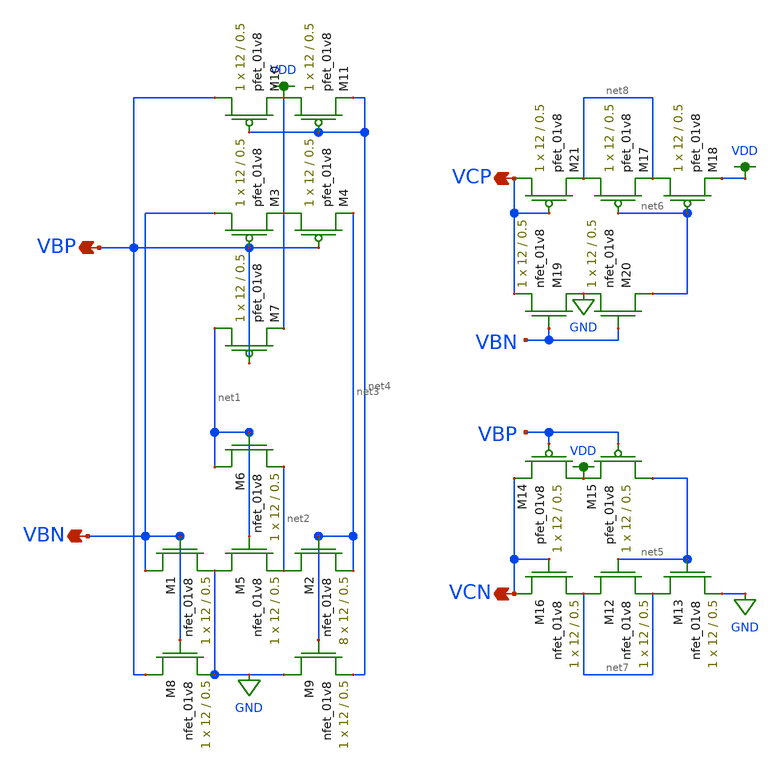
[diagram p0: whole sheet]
** sch_path: miniproject_03/xschem/bias_gen_layout.sch
**.subckt bias_gen_layout VBP VBN VCP VCN
*.opin VBP
*.opin VBN
*.opin VCP
*.opin VCN
XM2 net2 net3 net3 GND sky130_fd_pr__nfet_01v8 L=0.5 W=12 nf=1 ad='int((nf+1)/2) * W/nf * 0.29' as='int((nf+2)/2) * W/nf * 0.29'
+ pd='2*int((nf+1)/2) * (W/nf + 0.29)' ps='2*int((nf+2)/2) * (W/nf + 0.29)' nrd='0.29 / W' nrs='0.29 / W'
+ sa=0 sb=0 sd=0 mult=8 m=8
XM11 VDD net4 net4 VDD sky130_fd_pr__pfet_01v8 L=0.5 W=12 nf=1 ad='int((nf+1)/2) * W/nf * 0.29' as='int((nf+2)/2) * W/nf * 0.29'
+ pd='2*int((nf+1)/2) * (W/nf + 0.29)' ps='2*int((nf+2)/2) * (W/nf + 0.29)' nrd='0.29 / W' nrs='0.29 / W'
+ sa=0 sb=0 sd=0 mult=1 m=1
XM1 VBN VBN GND GND sky130_fd_pr__nfet_01v8 L=0.5 W=12 nf=1 ad='int((nf+1)/2) * W/nf * 0.29' as='int((nf+2)/2) * W/nf * 0.29'
+ pd='2*int((nf+1)/2) * (W/nf + 0.29)' ps='2*int((nf+2)/2) * (W/nf + 0.29)' nrd='0.29 / W' nrs='0.29 / W'
+ sa=0 sb=0 sd=0 mult=1 m=1
XM4 VDD VBP net3 VDD sky130_fd_pr__pfet_01v8 L=0.5 W=12 nf=1 ad='int((nf+1)/2) * W/nf * 0.29' as='int((nf+2)/2) * W/nf * 0.29'
+ pd='2*int((nf+1)/2) * (W/nf + 0.29)' ps='2*int((nf+2)/2) * (W/nf + 0.29)' nrd='0.29 / W' nrs='0.29 / W'
+ sa=0 sb=0 sd=0 mult=1 m=1
XM10 VBP net4 VDD VDD sky130_fd_pr__pfet_01v8 L=0.5 W=12 nf=1 ad='int((nf+1)/2) * W/nf * 0.29' as='int((nf+2)/2) * W/nf * 0.29'
+ pd='2*int((nf+1)/2) * (W/nf + 0.29)' ps='2*int((nf+2)/2) * (W/nf + 0.29)' nrd='0.29 / W' nrs='0.29 / W'
+ sa=0 sb=0 sd=0 mult=1 m=1
XM3 VBN VBP VDD VDD sky130_fd_pr__pfet_01v8 L=0.5 W=12 nf=1 ad='int((nf+1)/2) * W/nf * 0.29' as='int((nf+2)/2) * W/nf * 0.29'
+ pd='2*int((nf+1)/2) * (W/nf + 0.29)' ps='2*int((nf+2)/2) * (W/nf + 0.29)' nrd='0.29 / W' nrs='0.29 / W'
+ sa=0 sb=0 sd=0 mult=1 m=1
XM8 VBP VBN GND GND sky130_fd_pr__nfet_01v8 L=0.5 W=12 nf=1 ad='int((nf+1)/2) * W/nf * 0.29' as='int((nf+2)/2) * W/nf * 0.29'
+ pd='2*int((nf+1)/2) * (W/nf + 0.29)' ps='2*int((nf+2)/2) * (W/nf + 0.29)' nrd='0.29 / W' nrs='0.29 / W'
+ sa=0 sb=0 sd=0 mult=1 m=1
XM9 GND net3 net4 GND sky130_fd_pr__nfet_01v8 L=0.5 W=12 nf=1 ad='int((nf+1)/2) * W/nf * 0.29' as='int((nf+2)/2) * W/nf * 0.29'
+ pd='2*int((nf+1)/2) * (W/nf + 0.29)' ps='2*int((nf+2)/2) * (W/nf + 0.29)' nrd='0.29 / W' nrs='0.29 / W'
+ sa=0 sb=0 sd=0 mult=1 m=1
XM6 net1 net1 net2 GND sky130_fd_pr__nfet_01v8 L=0.5 W=12 nf=1 ad='int((nf+1)/2) * W/nf * 0.29' as='int((nf+2)/2) * W/nf * 0.29'
+ pd='2*int((nf+1)/2) * (W/nf + 0.29)' ps='2*int((nf+2)/2) * (W/nf + 0.29)' nrd='0.29 / W' nrs='0.29 / W'
+ sa=0 sb=0 sd=0 mult=1 m=1
XM5 GND net1 net2 GND sky130_fd_pr__nfet_01v8 L=0.5 W=12 nf=1 ad='int((nf+1)/2) * W/nf * 0.29' as='int((nf+2)/2) * W/nf * 0.29'
+ pd='2*int((nf+1)/2) * (W/nf + 0.29)' ps='2*int((nf+2)/2) * (W/nf + 0.29)' nrd='0.29 / W' nrs='0.29 / W'
+ sa=0 sb=0 sd=0 mult=1 m=1
XM7 net1 VBP VDD VDD sky130_fd_pr__pfet_01v8 L=0.5 W=12 nf=1 ad='int((nf+1)/2) * W/nf * 0.29' as='int((nf+2)/2) * W/nf * 0.29'
+ pd='2*int((nf+1)/2) * (W/nf + 0.29)' ps='2*int((nf+2)/2) * (W/nf + 0.29)' nrd='0.29 / W' nrs='0.29 / W'
+ sa=0 sb=0 sd=0 mult=1 m=1
XM12 net7 net5 net7 GND sky130_fd_pr__nfet_01v8 L=0.5 W=12 nf=1 ad='int((nf+1)/2) * W/nf * 0.29' as='int((nf+2)/2) * W/nf * 0.29'
+ pd='2*int((nf+1)/2) * (W/nf + 0.29)' ps='2*int((nf+2)/2) * (W/nf + 0.29)' nrd='0.29 / W' nrs='0.29 / W'
+ sa=0 sb=0 sd=0 mult=1 m=1
XM14 VDD VBP VCN VDD sky130_fd_pr__pfet_01v8 L=0.5 W=12 nf=1 ad='int((nf+1)/2) * W/nf * 0.29' as='int((nf+2)/2) * W/nf * 0.29'
+ pd='2*int((nf+1)/2) * (W/nf + 0.29)' ps='2*int((nf+2)/2) * (W/nf + 0.29)' nrd='0.29 / W' nrs='0.29 / W'
+ sa=0 sb=0 sd=0 mult=1 m=1
XM13 net7 net5 GND GND sky130_fd_pr__nfet_01v8 L=0.5 W=12 nf=1 ad='int((nf+1)/2) * W/nf * 0.29' as='int((nf+2)/2) * W/nf * 0.29'
+ pd='2*int((nf+1)/2) * (W/nf + 0.29)' ps='2*int((nf+2)/2) * (W/nf + 0.29)' nrd='0.29 / W' nrs='0.29 / W'
+ sa=0 sb=0 sd=0 mult=1 m=1
XM15 net5 VBP VDD VDD sky130_fd_pr__pfet_01v8 L=0.5 W=12 nf=1 ad='int((nf+1)/2) * W/nf * 0.29' as='int((nf+2)/2) * W/nf * 0.29'
+ pd='2*int((nf+1)/2) * (W/nf + 0.29)' ps='2*int((nf+2)/2) * (W/nf + 0.29)' nrd='0.29 / W' nrs='0.29 / W'
+ sa=0 sb=0 sd=0 mult=1 m=1
XM16 VCN VCN net7 GND sky130_fd_pr__nfet_01v8 L=0.5 W=12 nf=1 ad='int((nf+1)/2) * W/nf * 0.29' as='int((nf+2)/2) * W/nf * 0.29'
+ pd='2*int((nf+1)/2) * (W/nf + 0.29)' ps='2*int((nf+2)/2) * (W/nf + 0.29)' nrd='0.29 / W' nrs='0.29 / W'
+ sa=0 sb=0 sd=0 mult=1 m=1
XM17 net8 net6 net8 VDD sky130_fd_pr__pfet_01v8 L=0.5 W=12 nf=1 ad='int((nf+1)/2) * W/nf * 0.29' as='int((nf+2)/2) * W/nf * 0.29'
+ pd='2*int((nf+1)/2) * (W/nf + 0.29)' ps='2*int((nf+2)/2) * (W/nf + 0.29)' nrd='0.29 / W' nrs='0.29 / W'
+ sa=0 sb=0 sd=0 mult=1 m=1
XM18 net8 net6 VDD VDD sky130_fd_pr__pfet_01v8 L=0.5 W=12 nf=1 ad='int((nf+1)/2) * W/nf * 0.29' as='int((nf+2)/2) * W/nf * 0.29'
+ pd='2*int((nf+1)/2) * (W/nf + 0.29)' ps='2*int((nf+2)/2) * (W/nf + 0.29)' nrd='0.29 / W' nrs='0.29 / W'
+ sa=0 sb=0 sd=0 mult=1 m=1
XM19 GND VBN VCP GND sky130_fd_pr__nfet_01v8 L=0.5 W=12 nf=1 ad='int((nf+1)/2) * W/nf * 0.29' as='int((nf+2)/2) * W/nf * 0.29'
+ pd='2*int((nf+1)/2) * (W/nf + 0.29)' ps='2*int((nf+2)/2) * (W/nf + 0.29)' nrd='0.29 / W' nrs='0.29 / W'
+ sa=0 sb=0 sd=0 mult=1 m=1
XM20 net6 VBN GND GND sky130_fd_pr__nfet_01v8 L=0.5 W=12 nf=1 ad='int((nf+1)/2) * W/nf * 0.29' as='int((nf+2)/2) * W/nf * 0.29'
+ pd='2*int((nf+1)/2) * (W/nf + 0.29)' ps='2*int((nf+2)/2) * (W/nf + 0.29)' nrd='0.29 / W' nrs='0.29 / W'
+ sa=0 sb=0 sd=0 mult=1 m=1
XM21 VCP VCP net8 VDD sky130_fd_pr__pfet_01v8 L=0.5 W=12 nf=1 ad='int((nf+1)/2) * W/nf * 0.29' as='int((nf+2)/2) * W/nf * 0.29'
+ pd='2*int((nf+1)/2) * (W/nf + 0.29)' ps='2*int((nf+2)/2) * (W/nf + 0.29)' nrd='0.29 / W' nrs='0.29 / W'
+ sa=0 sb=0 sd=0 mult=1 m=1
**.ends
.GLOBAL VDD
.GLOBAL GND
.end
